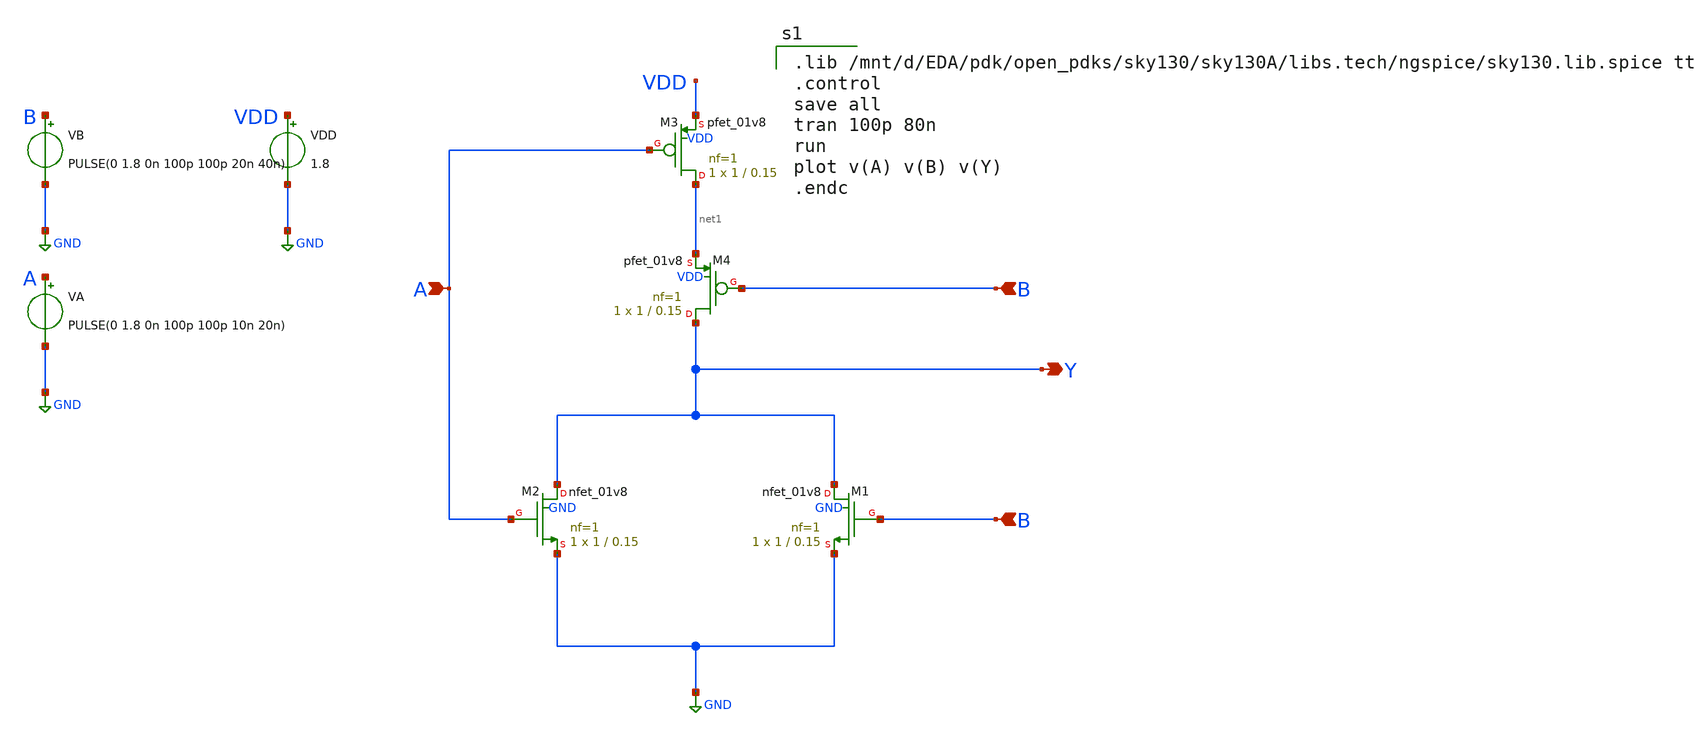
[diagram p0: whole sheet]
** sch_path: nor/nor.sch
**.subckt nor A B Y B
*.ipin A
*.ipin B
*.opin Y
*.ipin B
XM1 Y B GND GND sky130_fd_pr__nfet_01v8 L=0.15 W=1 nf=1 ad='int((1 + 1)/2) * 1 / 1 * 0.29' as='int((1 + 2)/2) * 1 / 1 * 0.29'
+ pd='2*int((1 + 1)/2) * (1 / 1 + 0.29)' ps='2*int((1 + 2)/2) * (1 / 1 + 0.29)' nrd='0.29 / 1 ' nrs='0.29 / 1 '
+ sa=0 sb=0 sd=0 mult=1 m=1
XM2 Y A GND GND sky130_fd_pr__nfet_01v8 L=0.15 W=1 nf=1 ad='int((1 + 1)/2) * 1 / 1 * 0.29' as='int((1 + 2)/2) * 1 / 1 * 0.29'
+ pd='2*int((1 + 1)/2) * (1 / 1 + 0.29)' ps='2*int((1 + 2)/2) * (1 / 1 + 0.29)' nrd='0.29 / 1 ' nrs='0.29 / 1 '
+ sa=0 sb=0 sd=0 mult=1 m=1
VDD VDD GND 1.8
VA A GND PULSE(0 1.8 0n 100p 100p 10n 20n)
VB B GND PULSE(0 1.8 0n 100p 100p 20n 40n)
XM3 net1 A VDD VDD sky130_fd_pr__pfet_01v8 L=0.15 W=1 nf=1 ad='int((1 + 1)/2) * 1 / 1 * 0.29' as='int((1 + 2)/2) * 1 / 1 * 0.29'
+ pd='2*int((1 + 1)/2) * (1 / 1 + 0.29)' ps='2*int((1 + 2)/2) * (1 / 1 + 0.29)' nrd='0.29 / 1 ' nrs='0.29 / 1 '
+ sa=0 sb=0 sd=0 mult=1 m=1
XM4 Y B net1 VDD sky130_fd_pr__pfet_01v8 L=0.15 W=1 nf=1 ad='int((1 + 1)/2) * 1 / 1 * 0.29' as='int((1 + 2)/2) * 1 / 1 * 0.29'
+ pd='2*int((1 + 1)/2) * (1 / 1 + 0.29)' ps='2*int((1 + 2)/2) * (1 / 1 + 0.29)' nrd='0.29 / 1 ' nrs='0.29 / 1 '
+ sa=0 sb=0 sd=0 mult=1 m=1
**** begin user architecture code

.lib /mnt/d/EDA/pdk/open_pdks/sky130/sky130A/libs.tech/ngspice/sky130.lib.spice tt
.control
save all
tran 100p 80n
run
plot v(A) v(B) v(Y)
.endc

**** end user architecture code
**.ends
.GLOBAL GND
.end
